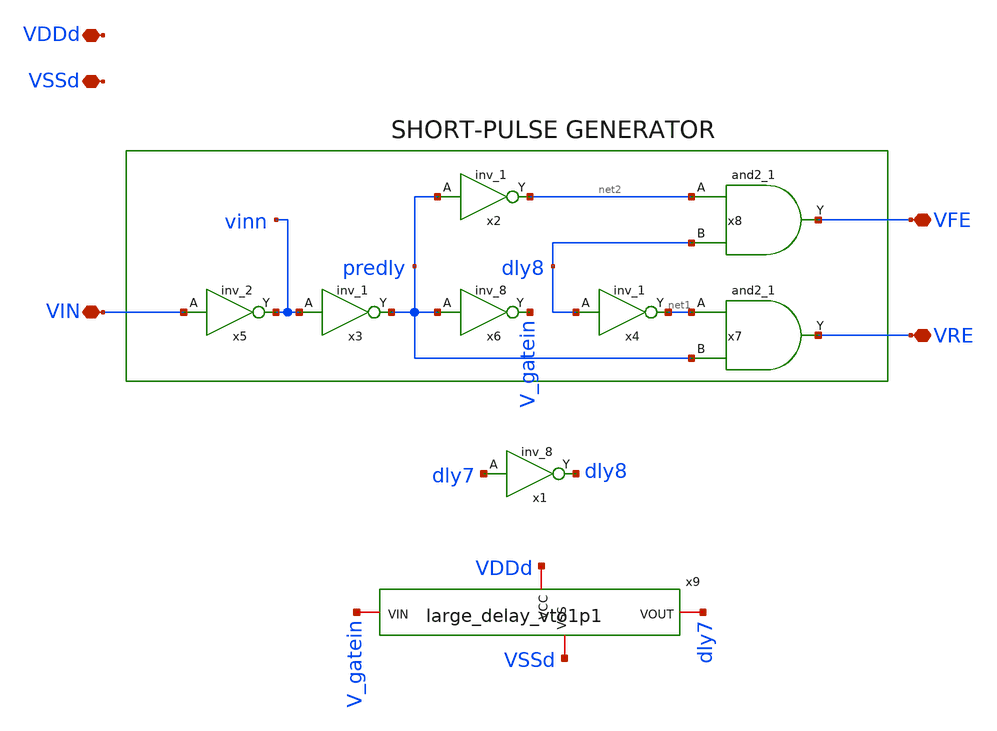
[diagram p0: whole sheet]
** sch_path: xschem/gf180_digital/SPG/SPG_vto1p1.sch
**.subckt SPG_vto1p1 VIN VFE VRE VDDd VSSd
*.iopin VIN
*.iopin VFE
*.iopin VRE
*.iopin VDDd
*.iopin VSSd
x2 predly VSSd VDDd VSSd VDDd net2 gf180mcu_fd_sc_mcu9t5v0__inv_1
x3 vinn VSSd VDDd VSSd VDDd predly gf180mcu_fd_sc_mcu9t5v0__inv_1
x4 dly8 VSSd VDDd VSSd VDDd net1 gf180mcu_fd_sc_mcu9t5v0__inv_1
x5 VIN VSSd VDDd VSSd VDDd vinn gf180mcu_fd_sc_mcu9t5v0__inv_2
x6 predly VSSd VDDd VSSd VDDd V_gatein gf180mcu_fd_sc_mcu9t5v0__inv_8
x9 VDDd VSSd V_gatein dly7 large_delay_vto1p1
x1 dly7 VSSd VDDd VSSd VDDd dly8 gf180mcu_fd_sc_mcu9t5v0__inv_8
x8 net2 dly8 VFE VDDd VDDd VSSd VSSd gf180mcu_fd_sc_mcu9t5v0__and2_1
x7 net1 predly VRE VDDd VDDd VSSd VSSd gf180mcu_fd_sc_mcu9t5v0__and2_1
**.ends

* expanding   symbol:  gf180_digital/large_delay/large_delay_vto1p1.sym # of pins=4
** sym_path: xschem/gf180_digital/large_delay/large_delay_vto1p1.sym
** sch_path: xschem/gf180_digital/large_delay/large_delay_vto1p1.sch
.subckt large_delay_vto1p1 VDDd VSSd VIN VOUT
*.iopin VIN
*.iopin VOUT
*.iopin VDDd
*.iopin VSSd
x1 VIN VOUT VDDd VDDd VSSd VSSd gf180mcu_fd_sc_mcu9t5v0__dlya_1
.ends

.end
